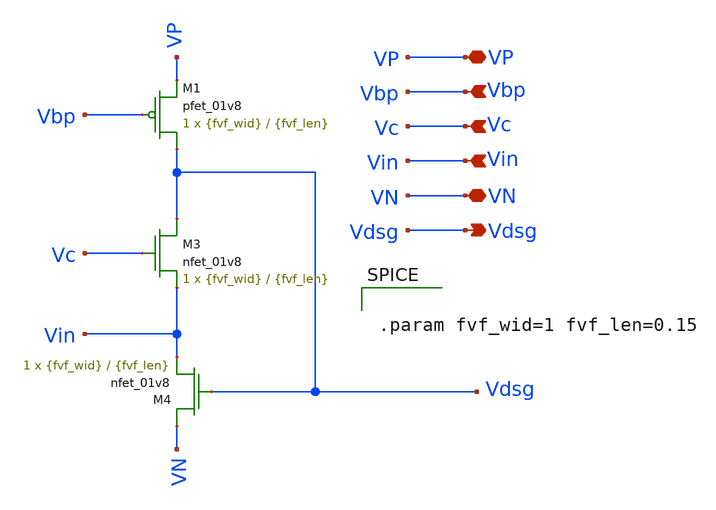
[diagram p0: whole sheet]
** sch_path: fvf.sch
**.subckt fvf VP Vbp Vc Vin VN Vdsg
*.iopin VP
*.ipin Vbp
*.ipin Vc
*.ipin Vin
*.iopin VN
*.opin Vdsg
XM3 Vdsg Vc Vin VN sky130_fd_pr__nfet_01v8 L={fvf_len} W={fvf_wid} nf=1 ad='int((nf+1)/2) * W/nf * 0.29'
+ as='int((nf+2)/2) * W/nf * 0.29' pd='2*int((nf+1)/2) * (W/nf + 0.29)' ps='2*int((nf+2)/2) * (W/nf + 0.29)'
+ nrd='0.29 / W' nrs='0.29 / W' sa=0 sb=0 sd=0 mult=1 m=1
XM4 VN Vdsg Vin VN sky130_fd_pr__nfet_01v8 L={fvf_len} W={fvf_wid} nf=1 ad='int((nf+1)/2) * W/nf * 0.29'
+ as='int((nf+2)/2) * W/nf * 0.29' pd='2*int((nf+1)/2) * (W/nf + 0.29)' ps='2*int((nf+2)/2) * (W/nf + 0.29)'
+ nrd='0.29 / W' nrs='0.29 / W' sa=0 sb=0 sd=0 mult=1 m=1
XM1 Vdsg Vbp VP VP sky130_fd_pr__pfet_01v8 L={fvf_len} W={fvf_wid} nf=1 ad='int((nf+1)/2) * W/nf * 0.29'
+ as='int((nf+2)/2) * W/nf * 0.29' pd='2*int((nf+1)/2) * (W/nf + 0.29)' ps='2*int((nf+2)/2) * (W/nf + 0.29)'
+ nrd='0.29 / W' nrs='0.29 / W' sa=0 sb=0 sd=0 mult=1 m=1
**** begin user architecture code


.param fvf_wid=1 fvf_len=0.15


**** end user architecture code
**.ends
.end
